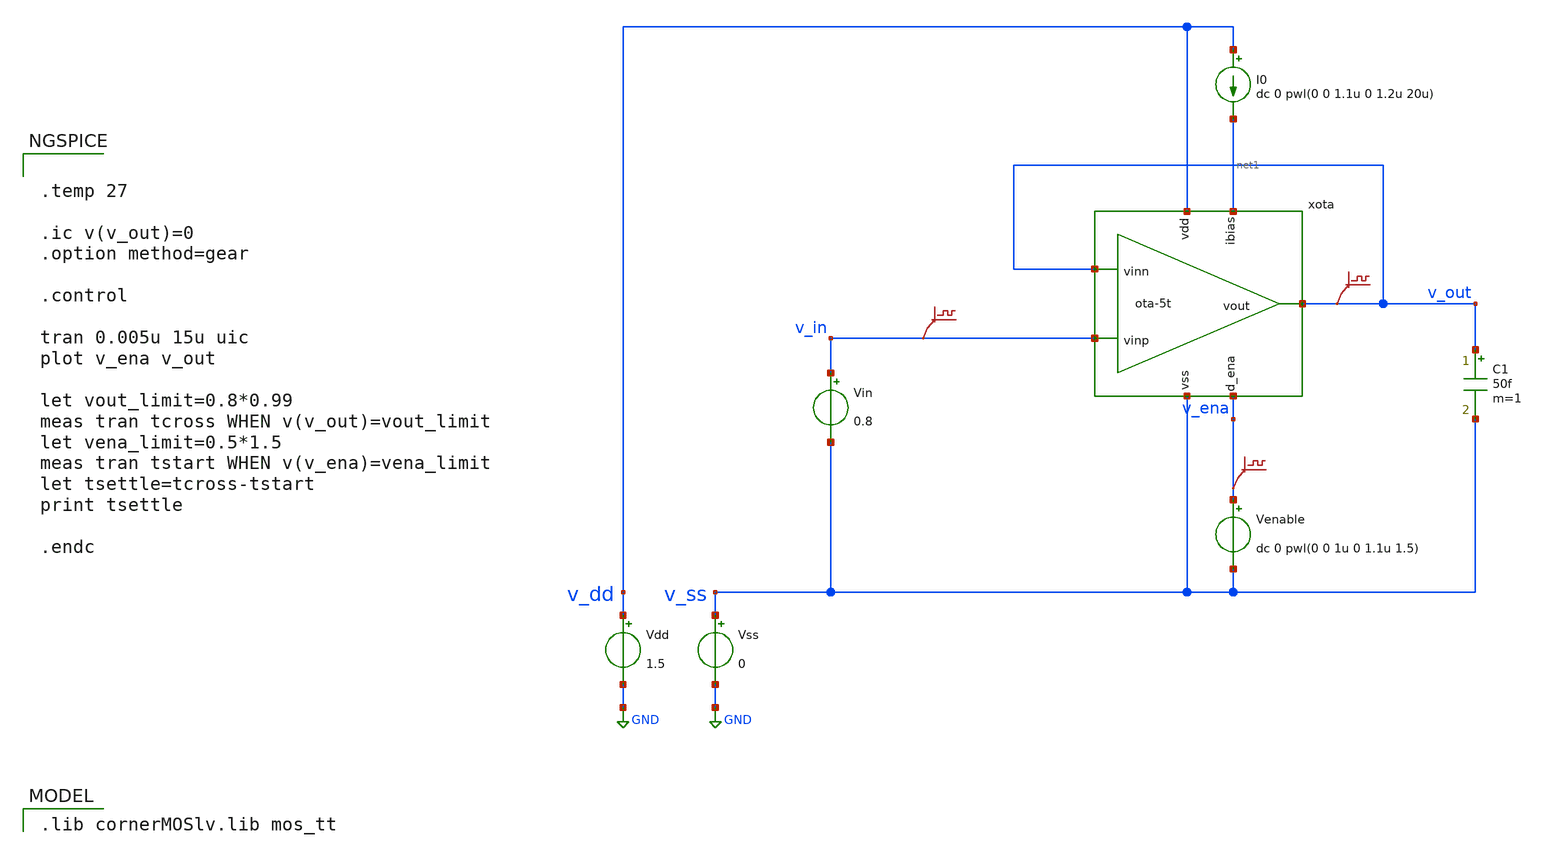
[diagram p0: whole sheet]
** sch_path: prj/template/3_Real_circuits/ota-5t_tb-tran.sch
* (c) 2024-2025 H. Pretl, Apache-2.0 license
**.subckt ota-5t_tb-tran
Vdd v_dd GND 1.5
xota v_dd v_out v_out v_in net1 v_ena v_ss ota-5t
Vss v_ss GND 0
C1 v_out v_ss 50f m=1
Vin v_in v_ss 0.8
I0 v_dd net1 dc 0 pwl(0 0 1.1u 0 1.2u 20u)
Venable v_ena v_ss dc 0 pwl(0 0 1u 0 1.1u 1.5)
.save v(v_in)
.save v(v_out)
.save v(v_ena)
**** begin user architecture code
 .lib cornerMOSlv.lib mos_tt



.temp 27

.ic v(v_out)=0
.option method=gear

.control

tran 0.005u 15u uic
plot v_ena v_out

let vout_limit=0.8*0.99
meas tran tcross WHEN v(v_out)=vout_limit
let vena_limit=0.5*1.5
meas tran tstart WHEN v(v_ena)=vena_limit
let tsettle=tcross-tstart
print tsettle

.endc


**** end user architecture code
**.ends

* expanding   symbol:  ota-5t.sym # of pins=7
** sym_path: prj/template/3_Real_circuits/ota-5t.sym
** sch_path: prj/template/3_Real_circuits/ota-5t.sch
.subckt ota-5t vdd vout vinn vinp ibias d_ena vss
*.ipin ibias
*.iopin vdd
*.iopin vss
*.ipin vinp
*.ipin vinn
*.opin vout
*.ipin d_ena
XM5 tail gate_n vss vss sg13_lv_nmos w=0.5u l=5u ng=1 m=1 mm_ok=1
XM4 vout gate_p vdd vdd sg13_lv_pmos w=1.5u l=5u ng=1 m=1 mm_ok=1
XM1 gate_p vinp tail vss sg13_lv_nmos w=2u l=5u ng=1 m=1 mm_ok=1
XM2 vout vinn tail vss sg13_lv_nmos w=2u l=5u ng=1 m=1 mm_ok=1
XM3 gate_p gate_p vdd vdd sg13_lv_pmos w=1.5u l=5u ng=1 m=1 mm_ok=1
XM6 ibias gate_n vss vss sg13_lv_nmos w=2.5u l=5u ng=5 m=1 mm_ok=1
XM9 gate_n ena_n vss vss sg13_lv_nmos w=0.5u l=0.13u ng=1 m=1 mm_ok=1
XM11 gate_p ena vdd vdd sg13_lv_pmos w=1.5u l=0.13u ng=1 m=1 mm_ok=1
XM7 ena ena_n vss vss sg13_lv_nmos w=0.5u l=0.13u ng=1 m=1 mm_ok=1
XM8 ena ena_n vdd vdd sg13_lv_pmos w=1.5u l=0.13u ng=1 m=1 mm_ok=1
XM10 ibias ena gate_n vss sg13_lv_nmos w=0.5u l=0.13u ng=1 m=1 mm_ok=1
XM12 ena_n d_ena vss vss sg13_lv_nmos w=0.5u l=0.13u ng=1 m=1 mm_ok=1
XM13 ena_n d_ena vdd vdd sg13_lv_pmos w=1.5u l=0.13u ng=1 m=1 mm_ok=1
.ends

.GLOBAL GND
.end
